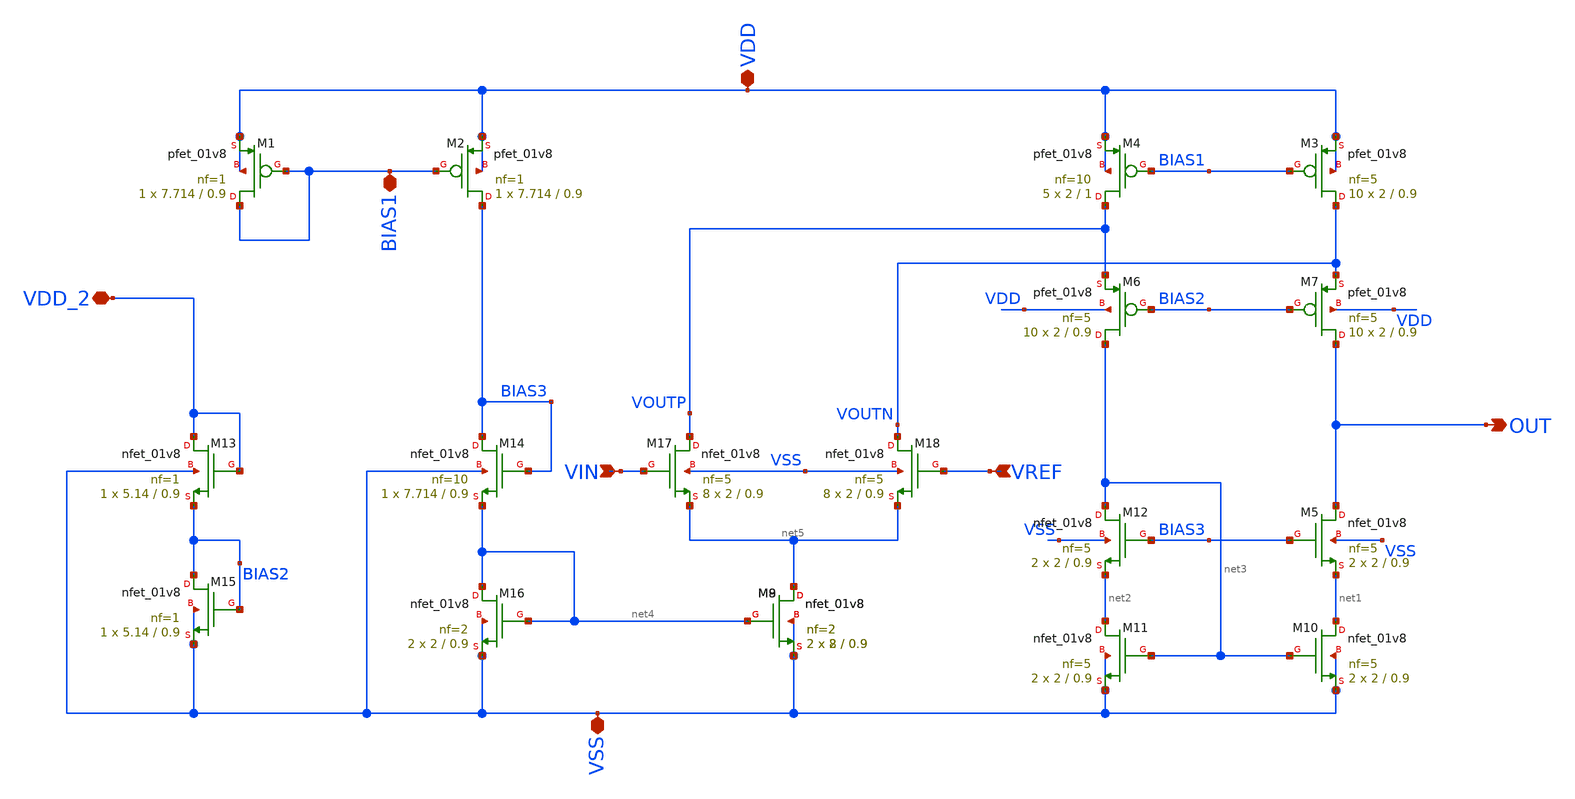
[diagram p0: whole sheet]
** sch_path: xschem/DC_DC_Converter_xschem/OTHERS/DC_DC_Converter_JV10/Folded_OPAMP_v2/Folded_OPAMP.sch
**.subckt Folded_OPAMP VSS VDD VDD_2 OUT VIN VREF BIAS1
*.iopin VSS
*.iopin VDD
*.iopin VDD_2
*.opin OUT
*.ipin VIN
*.ipin VREF
*.iopin BIAS1
XM13 VDD_2 VDD_2 BIAS2 VSS sky130_fd_pr__nfet_01v8 L=0.9 W=5.14 nf=1 ad='int((nf+1)/2) * W/nf * 0.29'
+ as='int((nf+2)/2) * W/nf * 0.29' pd='2*int((nf+1)/2) * (W/nf + 0.29)' ps='2*int((nf+2)/2) * (W/nf + 0.29)'
+ nrd='0.29 / W' nrs='0.29 / W' sa=0 sb=0 sd=0 mult=1 m=1
XM14 BIAS3 BIAS3 net4 VSS sky130_fd_pr__nfet_01v8 L=0.9 W=7.714 nf=10 ad='int((nf+1)/2) * W/nf * 0.29'
+ as='int((nf+2)/2) * W/nf * 0.29' pd='2*int((nf+1)/2) * (W/nf + 0.29)' ps='2*int((nf+2)/2) * (W/nf + 0.29)'
+ nrd='0.29 / W' nrs='0.29 / W' sa=0 sb=0 sd=0 mult=1 m=1
XM15 BIAS2 BIAS2 VSS VSS sky130_fd_pr__nfet_01v8 L=0.9 W=5.14 nf=1 ad='int((nf+1)/2) * W/nf * 0.29' as='int((nf+2)/2) * W/nf * 0.29'
+ pd='2*int((nf+1)/2) * (W/nf + 0.29)' ps='2*int((nf+2)/2) * (W/nf + 0.29)' nrd='0.29 / W' nrs='0.29 / W'
+ sa=0 sb=0 sd=0 mult=1 m=1
XM17 VOUTP VIN net5 VSS sky130_fd_pr__nfet_01v8 L=0.9 W=2 nf=5 ad='int((nf+1)/2) * W/nf * 0.29' as='int((nf+2)/2) * W/nf * 0.29'
+ pd='2*int((nf+1)/2) * (W/nf + 0.29)' ps='2*int((nf+2)/2) * (W/nf + 0.29)' nrd='0.29 / W' nrs='0.29 / W'
+ sa=0 sb=0 sd=0 mult=8 m=8
XM9 net5 net4 VSS VSS sky130_fd_pr__nfet_01v8 L=0.9 W=2 nf=2 ad='int((nf+1)/2) * W/nf * 0.29' as='int((nf+2)/2) * W/nf * 0.29'
+ pd='2*int((nf+1)/2) * (W/nf + 0.29)' ps='2*int((nf+2)/2) * (W/nf + 0.29)' nrd='0.29 / W' nrs='0.29 / W'
+ sa=0 sb=0 sd=0 mult=2 m=2
XM1 BIAS1 BIAS1 VDD VDD sky130_fd_pr__pfet_01v8 L=0.9 W=7.714 nf=1 ad='int((nf+1)/2) * W/nf * 0.29' as='int((nf+2)/2) * W/nf * 0.29'
+ pd='2*int((nf+1)/2) * (W/nf + 0.29)' ps='2*int((nf+2)/2) * (W/nf + 0.29)' nrd='0.29 / W' nrs='0.29 / W'
+ sa=0 sb=0 sd=0 mult=1 m=1
XM2 BIAS3 BIAS1 VDD VDD sky130_fd_pr__pfet_01v8 L=0.9 W=7.714 nf=1 ad='int((nf+1)/2) * W/nf * 0.29' as='int((nf+2)/2) * W/nf * 0.29'
+ pd='2*int((nf+1)/2) * (W/nf + 0.29)' ps='2*int((nf+2)/2) * (W/nf + 0.29)' nrd='0.29 / W' nrs='0.29 / W'
+ sa=0 sb=0 sd=0 mult=1 m=1
XM18 VOUTN VREF net5 VSS sky130_fd_pr__nfet_01v8 L=0.9 W=2 nf=5 ad='int((nf+1)/2) * W/nf * 0.29' as='int((nf+2)/2) * W/nf * 0.29'
+ pd='2*int((nf+1)/2) * (W/nf + 0.29)' ps='2*int((nf+2)/2) * (W/nf + 0.29)' nrd='0.29 / W' nrs='0.29 / W'
+ sa=0 sb=0 sd=0 mult=8 m=8
XM8 net5 net4 VSS VSS sky130_fd_pr__nfet_01v8 L=0.9 W=8 nf=2 ad='int((nf+1)/2) * W/nf * 0.29' as='int((nf+2)/2) * W/nf * 0.29'
+ pd='2*int((nf+1)/2) * (W/nf + 0.29)' ps='2*int((nf+2)/2) * (W/nf + 0.29)' nrd='0.29 / W' nrs='0.29 / W'
+ sa=0 sb=0 sd=0 mult=2 m=2
XM4 VOUTP BIAS1 VDD VDD sky130_fd_pr__pfet_01v8 L=1 W=2 nf=10 ad='int((nf+1)/2) * W/nf * 0.29' as='int((nf+2)/2) * W/nf * 0.29'
+ pd='2*int((nf+1)/2) * (W/nf + 0.29)' ps='2*int((nf+2)/2) * (W/nf + 0.29)' nrd='0.29 / W' nrs='0.29 / W'
+ sa=0 sb=0 sd=0 mult=5 m=5
XM3 VOUTN BIAS1 VDD VDD sky130_fd_pr__pfet_01v8 L=0.9 W=2 nf=5 ad='int((nf+1)/2) * W/nf * 0.29' as='int((nf+2)/2) * W/nf * 0.29'
+ pd='2*int((nf+1)/2) * (W/nf + 0.29)' ps='2*int((nf+2)/2) * (W/nf + 0.29)' nrd='0.29 / W' nrs='0.29 / W'
+ sa=0 sb=0 sd=0 mult=10 m=10
XM6 net3 BIAS2 VOUTP VDD sky130_fd_pr__pfet_01v8 L=0.9 W=2 nf=5 ad='int((nf+1)/2) * W/nf * 0.29' as='int((nf+2)/2) * W/nf * 0.29'
+ pd='2*int((nf+1)/2) * (W/nf + 0.29)' ps='2*int((nf+2)/2) * (W/nf + 0.29)' nrd='0.29 / W' nrs='0.29 / W'
+ sa=0 sb=0 sd=0 mult=10 m=10
XM7 OUT BIAS2 VOUTN VDD sky130_fd_pr__pfet_01v8 L=0.9 W=2 nf=5 ad='int((nf+1)/2) * W/nf * 0.29' as='int((nf+2)/2) * W/nf * 0.29'
+ pd='2*int((nf+1)/2) * (W/nf + 0.29)' ps='2*int((nf+2)/2) * (W/nf + 0.29)' nrd='0.29 / W' nrs='0.29 / W'
+ sa=0 sb=0 sd=0 mult=10 m=10
XM5 OUT BIAS3 net1 VSS sky130_fd_pr__nfet_01v8 L=0.9 W=2 nf=5 ad='int((nf+1)/2) * W/nf * 0.29' as='int((nf+2)/2) * W/nf * 0.29'
+ pd='2*int((nf+1)/2) * (W/nf + 0.29)' ps='2*int((nf+2)/2) * (W/nf + 0.29)' nrd='0.29 / W' nrs='0.29 / W'
+ sa=0 sb=0 sd=0 mult=2 m=2
XM10 net1 net3 VSS VSS sky130_fd_pr__nfet_01v8 L=0.9 W=2 nf=5 ad='int((nf+1)/2) * W/nf * 0.29' as='int((nf+2)/2) * W/nf * 0.29'
+ pd='2*int((nf+1)/2) * (W/nf + 0.29)' ps='2*int((nf+2)/2) * (W/nf + 0.29)' nrd='0.29 / W' nrs='0.29 / W'
+ sa=0 sb=0 sd=0 mult=2 m=2
XM11 net2 net3 VSS VSS sky130_fd_pr__nfet_01v8 L=0.9 W=2 nf=5 ad='int((nf+1)/2) * W/nf * 0.29' as='int((nf+2)/2) * W/nf * 0.29'
+ pd='2*int((nf+1)/2) * (W/nf + 0.29)' ps='2*int((nf+2)/2) * (W/nf + 0.29)' nrd='0.29 / W' nrs='0.29 / W'
+ sa=0 sb=0 sd=0 mult=2 m=2
XM12 net3 BIAS3 net2 VSS sky130_fd_pr__nfet_01v8 L=0.9 W=2 nf=5 ad='int((nf+1)/2) * W/nf * 0.29' as='int((nf+2)/2) * W/nf * 0.29'
+ pd='2*int((nf+1)/2) * (W/nf + 0.29)' ps='2*int((nf+2)/2) * (W/nf + 0.29)' nrd='0.29 / W' nrs='0.29 / W'
+ sa=0 sb=0 sd=0 mult=2 m=2
XM16 net4 net4 VSS VSS sky130_fd_pr__nfet_01v8 L=0.9 W=2 nf=2 ad='int((nf+1)/2) * W/nf * 0.29' as='int((nf+2)/2) * W/nf * 0.29'
+ pd='2*int((nf+1)/2) * (W/nf + 0.29)' ps='2*int((nf+2)/2) * (W/nf + 0.29)' nrd='0.29 / W' nrs='0.29 / W'
+ sa=0 sb=0 sd=0 mult=2 m=2
**.ends
.end
